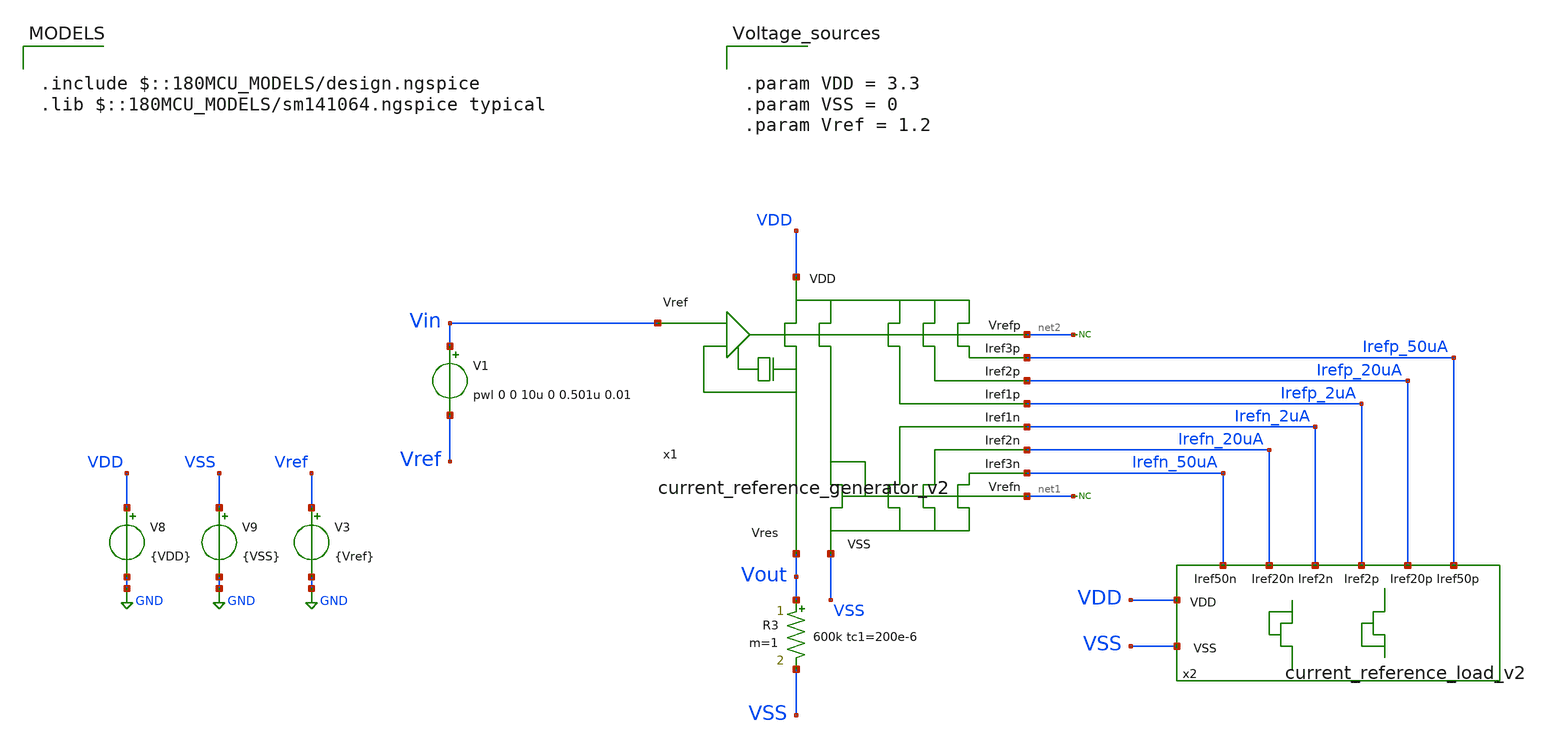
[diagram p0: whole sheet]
** sch_path: designs/libs/current_reference_generator_v2/xschem/current_reference_generator_v2_TB_tran.sch
**.subckt current_reference_generator_v2_TB_tran
V1 Vin Vref pwl 0 0 10u 0 0.501u 0.01
V8 VDD GND {VDD}
V9 VSS GND {VSS}
V3 Vref GND {Vref}
R3 Vout VSS 600k tc1=200e-6 m=1
* noconn #net1
* noconn #net2
x1 VSS VDD Vin net2 net1 Irefn_2uA Irefn_50uA Irefp_2uA Irefp_50uA Vout Irefn_20uA Irefp_20uA
+ current_reference_generator_v2
x2 Irefn_2uA Irefn_50uA Irefp_2uA Irefp_50uA VDD VSS Irefn_20uA Irefp_20uA current_reference_load_v2
**** begin user architecture code



.param VDD=1.8
.param Vref=1.2
.save


.control

    op

    * run tran simulation
    tran 1n 1.5u

    *let current_refp1 = v(Iref1p)/450e3

    plot v(Vout) v(Vin)

    write current_reference_generator_v2_TB_tran.raw
.endc




.include $::180MCU_MODELS/design.ngspice
.lib $::180MCU_MODELS/sm141064.ngspice typical



.param VDD = 3.3
.param VSS = 0
.param Vref = 1.2


**** end user architecture code
**.ends
.GLOBAL GND
.end
